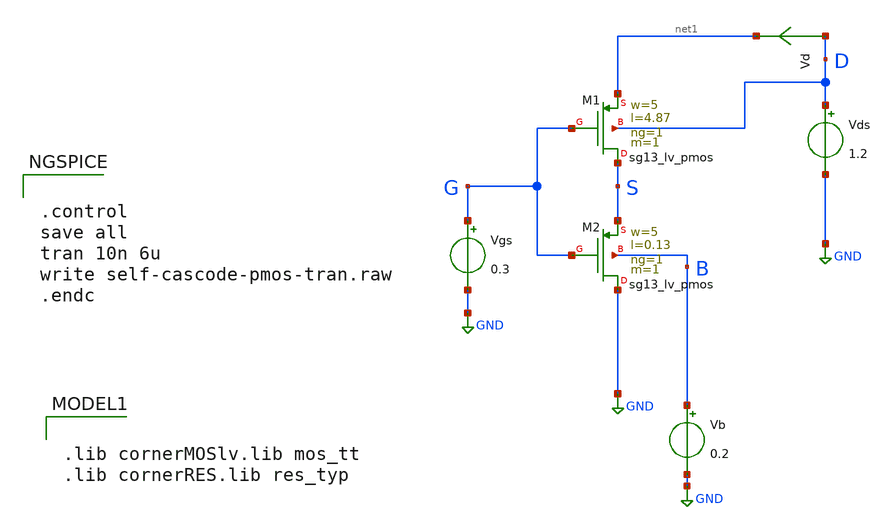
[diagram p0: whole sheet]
** sch_path: xschem/self-cascode-pmos-tran.sch
**.subckt self-cascode-pmos-tran
Vgs G GND 0.3
Vds D GND 1.2
Vd D net1 0
.save i(vd)
Vb B GND 0.2
XM1 S G net1 D sg13_lv_pmos w=5 l=4.87 ng=1 m=1 mm_ok=1
XM2 GND net2 S B sg13_lv_pmos w=5 l=0.13 ng=1 m=1 mm_ok=1
**** begin user architecture code


.control
save all
tran 10n 6u
write self-cascode-pmos-tran.raw
.endc



.lib cornerMOSlv.lib mos_tt
.lib cornerRES.lib res_typ

**** end user architecture code
**.ends
.GLOBAL GND
.end
